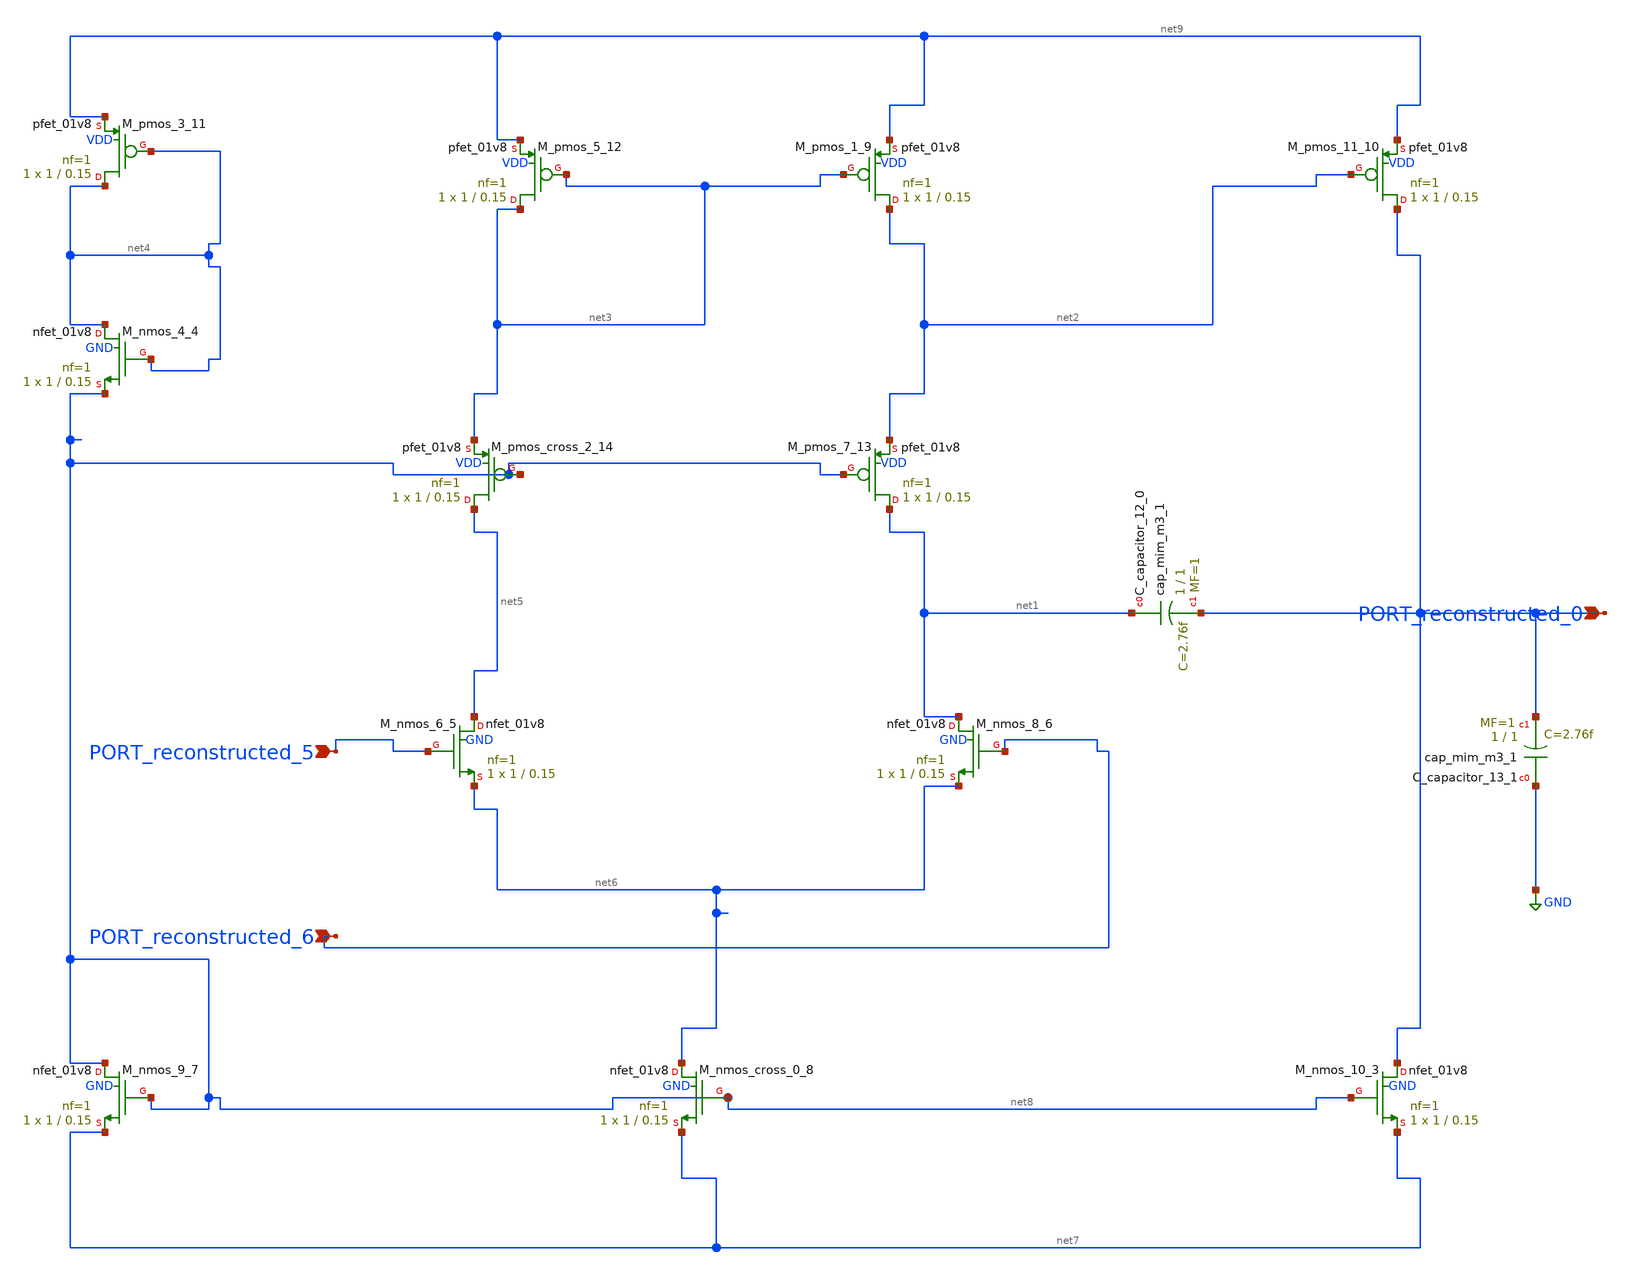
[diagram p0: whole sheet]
** sch_path: schematics/Image2Net/045.sch
**.subckt 045 PORT_reconstructed_5 PORT_reconstructed_6 PORT_reconstructed_0
*.ipin PORT_reconstructed_5
*.ipin PORT_reconstructed_6
*.ipin PORT_reconstructed_0
XC_capacitor_12_0 net1 PORT_reconstructed_0 sky130_fd_pr__cap_mim_m3_1 W=1 L=1 MF=1 m=1
XC_capacitor_13_1 GND PORT_reconstructed_0 sky130_fd_pr__cap_mim_m3_1 W=1 L=1 MF=1 m=1
XM_nmos_10_3 PORT_reconstructed_0 net8 net7 GND sky130_fd_pr__nfet_01v8 L=0.15 W=1 nf=1 ad='int((1 + 1)/2) * 1 / 1 * 0.29'
+ as='int((1 + 2)/2) * 1 / 1 * 0.29' pd='2*int((1 + 1)/2) * (1 / 1 + 0.29)' ps='2*int((1 + 2)/2) * (1 / 1 + 0.29)'
+ nrd='0.29 / 1 ' nrs='0.29 / 1 ' sa=0 sb=0 sd=0 mult=1 m=1
XM_nmos_4_4 net4 net4 net8 GND sky130_fd_pr__nfet_01v8 L=0.15 W=1 nf=1 ad='int((1 + 1)/2) * 1 / 1 * 0.29'
+ as='int((1 + 2)/2) * 1 / 1 * 0.29' pd='2*int((1 + 1)/2) * (1 / 1 + 0.29)' ps='2*int((1 + 2)/2) * (1 / 1 + 0.29)'
+ nrd='0.29 / 1 ' nrs='0.29 / 1 ' sa=0 sb=0 sd=0 mult=1 m=1
XM_nmos_6_5 net5 PORT_reconstructed_5 net6 GND sky130_fd_pr__nfet_01v8 L=0.15 W=1 nf=1 ad='int((1 + 1)/2) * 1 / 1 * 0.29'
+ as='int((1 + 2)/2) * 1 / 1 * 0.29' pd='2*int((1 + 1)/2) * (1 / 1 + 0.29)' ps='2*int((1 + 2)/2) * (1 / 1 + 0.29)'
+ nrd='0.29 / 1 ' nrs='0.29 / 1 ' sa=0 sb=0 sd=0 mult=1 m=1
XM_nmos_8_6 net1 PORT_reconstructed_6 net6 GND sky130_fd_pr__nfet_01v8 L=0.15 W=1 nf=1 ad='int((1 + 1)/2) * 1 / 1 * 0.29'
+ as='int((1 + 2)/2) * 1 / 1 * 0.29' pd='2*int((1 + 1)/2) * (1 / 1 + 0.29)' ps='2*int((1 + 2)/2) * (1 / 1 + 0.29)'
+ nrd='0.29 / 1 ' nrs='0.29 / 1 ' sa=0 sb=0 sd=0 mult=1 m=1
XM_nmos_9_7 net8 net8 net7 GND sky130_fd_pr__nfet_01v8 L=0.15 W=1 nf=1 ad='int((1 + 1)/2) * 1 / 1 * 0.29'
+ as='int((1 + 2)/2) * 1 / 1 * 0.29' pd='2*int((1 + 1)/2) * (1 / 1 + 0.29)' ps='2*int((1 + 2)/2) * (1 / 1 + 0.29)'
+ nrd='0.29 / 1 ' nrs='0.29 / 1 ' sa=0 sb=0 sd=0 mult=1 m=1
XM_nmos_cross_0_8 net6 net8 net7 GND sky130_fd_pr__nfet_01v8 L=0.15 W=1 nf=1 ad='int((1 + 1)/2) * 1 / 1 * 0.29'
+ as='int((1 + 2)/2) * 1 / 1 * 0.29' pd='2*int((1 + 1)/2) * (1 / 1 + 0.29)' ps='2*int((1 + 2)/2) * (1 / 1 + 0.29)'
+ nrd='0.29 / 1 ' nrs='0.29 / 1 ' sa=0 sb=0 sd=0 mult=1 m=1
XM_pmos_1_9 net2 net3 net9 VDD sky130_fd_pr__pfet_01v8 L=0.15 W=1 nf=1 ad='int((1 + 1)/2) * 1 / 1 * 0.29'
+ as='int((1 + 2)/2) * 1 / 1 * 0.29' pd='2*int((1 + 1)/2) * (1 / 1 + 0.29)' ps='2*int((1 + 2)/2) * (1 / 1 + 0.29)'
+ nrd='0.29 / 1 ' nrs='0.29 / 1 ' sa=0 sb=0 sd=0 mult=1 m=1
XM_pmos_11_10 PORT_reconstructed_0 net2 net9 VDD sky130_fd_pr__pfet_01v8 L=0.15 W=1 nf=1 ad='int((1 + 1)/2) * 1 / 1 * 0.29'
+ as='int((1 + 2)/2) * 1 / 1 * 0.29' pd='2*int((1 + 1)/2) * (1 / 1 + 0.29)' ps='2*int((1 + 2)/2) * (1 / 1 + 0.29)'
+ nrd='0.29 / 1 ' nrs='0.29 / 1 ' sa=0 sb=0 sd=0 mult=1 m=1
XM_pmos_3_11 net4 net4 net9 VDD sky130_fd_pr__pfet_01v8 L=0.15 W=1 nf=1 ad='int((1 + 1)/2) * 1 / 1 * 0.29'
+ as='int((1 + 2)/2) * 1 / 1 * 0.29' pd='2*int((1 + 1)/2) * (1 / 1 + 0.29)' ps='2*int((1 + 2)/2) * (1 / 1 + 0.29)'
+ nrd='0.29 / 1 ' nrs='0.29 / 1 ' sa=0 sb=0 sd=0 mult=1 m=1
XM_pmos_5_12 net3 net3 net9 VDD sky130_fd_pr__pfet_01v8 L=0.15 W=1 nf=1 ad='int((1 + 1)/2) * 1 / 1 * 0.29'
+ as='int((1 + 2)/2) * 1 / 1 * 0.29' pd='2*int((1 + 1)/2) * (1 / 1 + 0.29)' ps='2*int((1 + 2)/2) * (1 / 1 + 0.29)'
+ nrd='0.29 / 1 ' nrs='0.29 / 1 ' sa=0 sb=0 sd=0 mult=1 m=1
XM_pmos_7_13 net1 net8 net2 VDD sky130_fd_pr__pfet_01v8 L=0.15 W=1 nf=1 ad='int((1 + 1)/2) * 1 / 1 * 0.29'
+ as='int((1 + 2)/2) * 1 / 1 * 0.29' pd='2*int((1 + 1)/2) * (1 / 1 + 0.29)' ps='2*int((1 + 2)/2) * (1 / 1 + 0.29)'
+ nrd='0.29 / 1 ' nrs='0.29 / 1 ' sa=0 sb=0 sd=0 mult=1 m=1
XM_pmos_cross_2_14 net5 net8 net3 VDD sky130_fd_pr__pfet_01v8 L=0.15 W=1 nf=1 ad='int((1 + 1)/2) * 1 / 1 * 0.29'
+ as='int((1 + 2)/2) * 1 / 1 * 0.29' pd='2*int((1 + 1)/2) * (1 / 1 + 0.29)' ps='2*int((1 + 2)/2) * (1 / 1 + 0.29)'
+ nrd='0.29 / 1 ' nrs='0.29 / 1 ' sa=0 sb=0 sd=0 mult=1 m=1
**.ends
.GLOBAL GND
.end
